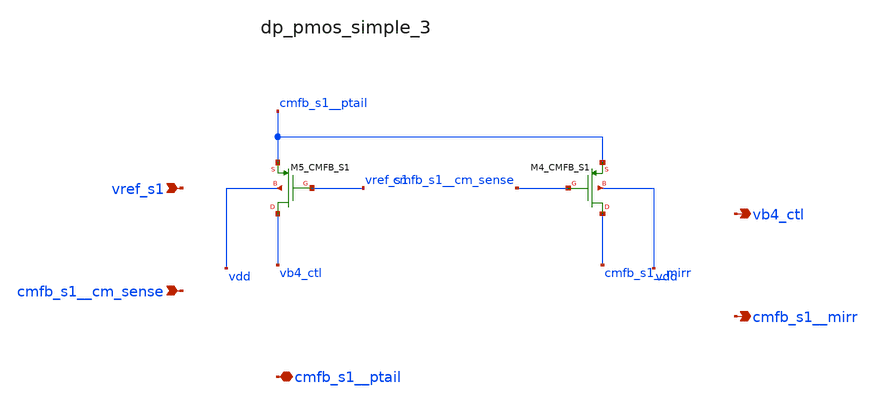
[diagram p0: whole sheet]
** sch_path: analog-db/raw/amp_035_fan_chopper_cmfb_dual/hier/blocks/dp_pmos_simple_3.sch
**.subckt dp_pmos_simple_3 vref_s1 cmfb_s1__cm_sense cmfb_s1__ptail vb4_ctl cmfb_s1__mirr
*.ipin vref_s1
*.ipin cmfb_s1__cm_sense
*.iopin cmfb_s1__ptail
*.opin vb4_ctl
*.opin cmfb_s1__mirr
XM4_CMFB_S1 cmfb_s1__mirr cmfb_s1__cm_sense cmfb_s1__ptail vdd sg13_lv_pmos w=x_dut_xm4_cmfb_s1_w
+ l=x_dut_xm4_cmfb_s1_l ng=1 m=x_dut_xm4_cmfb_s1_m
XM5_CMFB_S1 vb4_ctl vref_s1 cmfb_s1__ptail vdd sg13_lv_pmos w=x_dut_xm5_cmfb_s1_w
+ l=x_dut_xm5_cmfb_s1_l ng=1 m=x_dut_xm5_cmfb_s1_m
**.ends
.end
